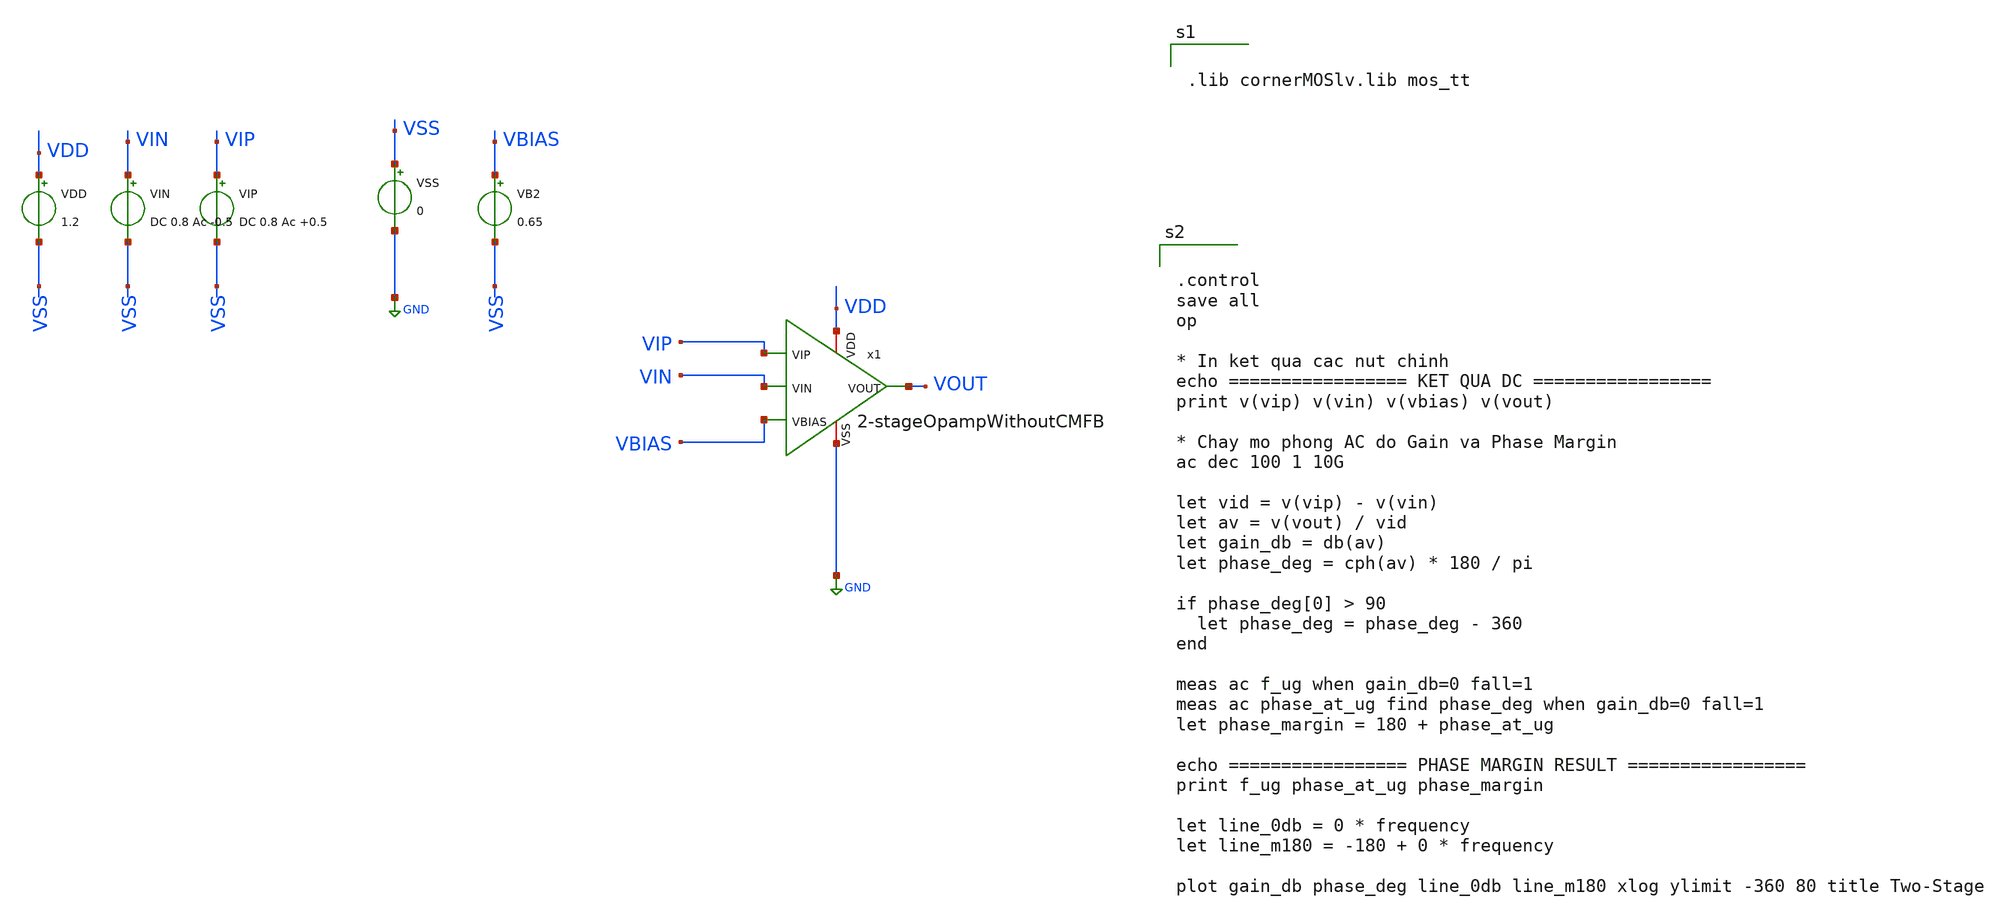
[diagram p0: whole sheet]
** sch_path: BTDay5-Ex/Test-full-diff_2-stage-OpampCore.sch
**.subckt Test-full-diff_2-stage-OpampCore
VDD VDD VSS 1.2
VIN VIN VSS DC 0.8 Ac -0.5
VIP VIP VSS DC 0.8 Ac +0.5
VSS VSS GND 0
VB2 VBIAS VSS 0.65
x1 VBIAS VOUT VIP VIN VDD GND 2-stageOpampWithoutCMFB
**** begin user architecture code


.lib cornerMOSlv.lib mos_tt




.control
save all
op

* In ket qua cac nut chinh
echo ================= KET QUA DC =================
print v(vip) v(vin) v(vbias) v(vout)

* Chay mo phong AC do Gain va Phase Margin
ac dec 100 1 10G

let vid = v(vip) - v(vin)
let av = v(vout) / vid
let gain_db = db(av)
let phase_deg = cph(av) * 180 / pi

if phase_deg[0] > 90
  let phase_deg = phase_deg - 360
end

meas ac f_ug when gain_db=0 fall=1
meas ac phase_at_ug find phase_deg when gain_db=0 fall=1
let phase_margin = 180 + phase_at_ug

echo ================= PHASE MARGIN RESULT =================
print f_ug phase_at_ug phase_margin

let line_0db = 0 * frequency
let line_m180 = -180 + 0 * frequency

plot gain_db phase_deg line_0db line_m180 xlog ylimit -360 80 title Two-Stage

**** end user architecture code
**.ends

* expanding   symbol:  /foss/designs/BTDay5-Ex/2-stageOpampWithoutCMFB.sym # of pins=6
** sym_path: BTDay5-Ex/2-stageOpampWithoutCMFB.sym
** sch_path: BTDay5-Ex/2-stageOpampWithoutCMFB.sch
.subckt 2-stageOpampWithoutCMFB VBIAS VOUT VIP VIN VDD VSS
*.iopin VSS
*.iopin VDD
*.ipin VIP
*.ipin VIN
*.ipin VBIAS
*.opin VOUT
XM1 net3 VIN net1 VSS sg13_lv_nmos w=4u l=1u ng=1 m=2 mm_ok=1
XM2 net4 VIP net1 VSS sg13_lv_nmos w=4u l=1u ng=1 m=2 mm_ok=1
XM3 net1 net2 VSS VSS sg13_lv_nmos w=4u l=1u ng=1 m=4 mm_ok=1
XM4 net3 net3 VDD VDD sg13_lv_pmos w=4u l=1u ng=1 m=2 mm_ok=1
XM7 net2 net2 VSS VSS sg13_lv_nmos w=4u l=1u ng=1 m=1 mm_ok=1
XM8 net2 VBIAS VDD VDD sg13_lv_pmos w=1u l=6u ng=1 m=1 mm_ok=1
XM10 net4 net3 VDD VDD sg13_lv_pmos w=4u l=1u ng=1 m=2 mm_ok=1
XM5 VOUT net2 VSS VSS sg13_lv_nmos w=4u l=1u ng=1 m=5 mm_ok=1
XM11 VOUT net4 VDD VDD sg13_lv_pmos w=4u l=1u ng=1 m=5 mm_ok=1
C2 VOUT net5 0.4p m=1
R1 net5 net4 150k m=1
.ends

.GLOBAL GND
.end
